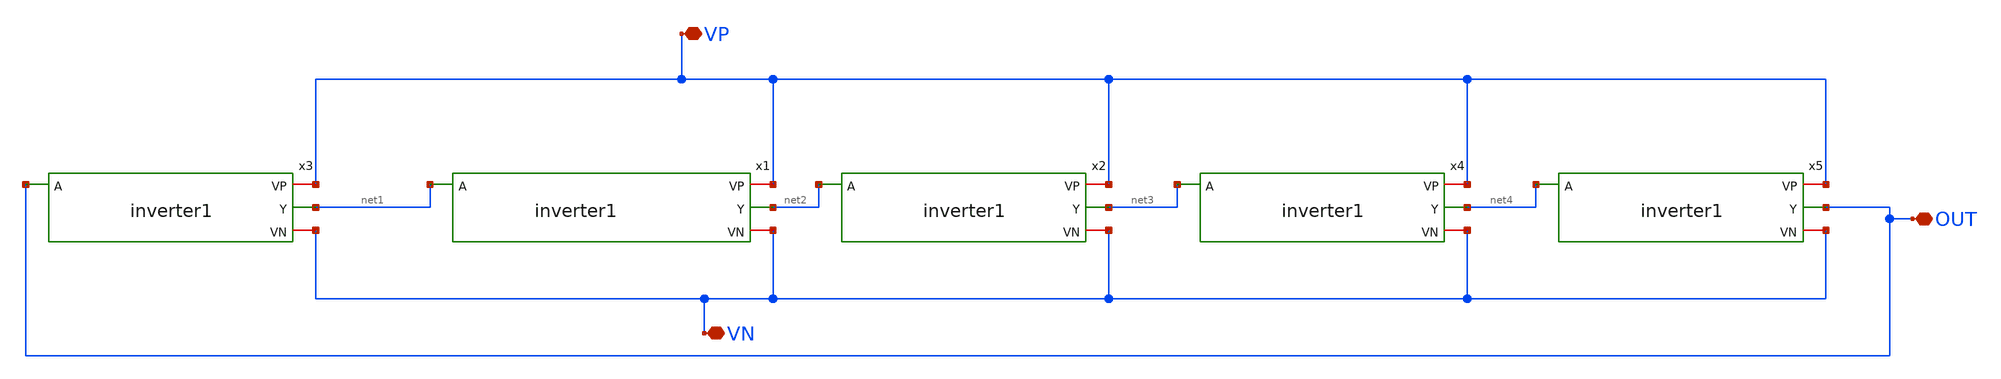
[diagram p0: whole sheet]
** sch_path: ring_oscillator.sch
**.subckt ring_oscillator VP VN OUT
*.iopin VP
*.iopin VN
*.iopin OUT
x1 VP net1 net2 VN inverter1
x2 VP net2 net3 VN inverter1
x3 VP OUT net1 VN inverter1
x4 VP net3 net4 VN inverter1
x5 VP net4 OUT VN inverter1
**.ends

* expanding   symbol:  inverter1.sym # of pins=4
** sym_path: inverter1.sym
** sch_path: inverter1.sch
.subckt inverter1 VP A Y VN
*.ipin A
*.opin Y
*.iopin VP
*.iopin VN
XM1 Y A VN VN sky130_fd_pr__nfet_01v8 L=1 W=0.5 nf=1 ad='int((nf+1)/2) * W/nf * 0.29' as='int((nf+2)/2) * W/nf * 0.29'
+ pd='2*int((nf+1)/2) * (W/nf + 0.29)' ps='2*int((nf+2)/2) * (W/nf + 0.29)' nrd='0.29 / W' nrs='0.29 / W'
+ sa=0 sb=0 sd=0 mult=1 m=1
XM2 Y A VP VP sky130_fd_pr__pfet_01v8 L=0.15 W=1 nf=1 ad='int((nf+1)/2) * W/nf * 0.29' as='int((nf+2)/2) * W/nf * 0.29'
+ pd='2*int((nf+1)/2) * (W/nf + 0.29)' ps='2*int((nf+2)/2) * (W/nf + 0.29)' nrd='0.29 / W' nrs='0.29 / W'
+ sa=0 sb=0 sd=0 mult=1 m=1
.ends

.end
